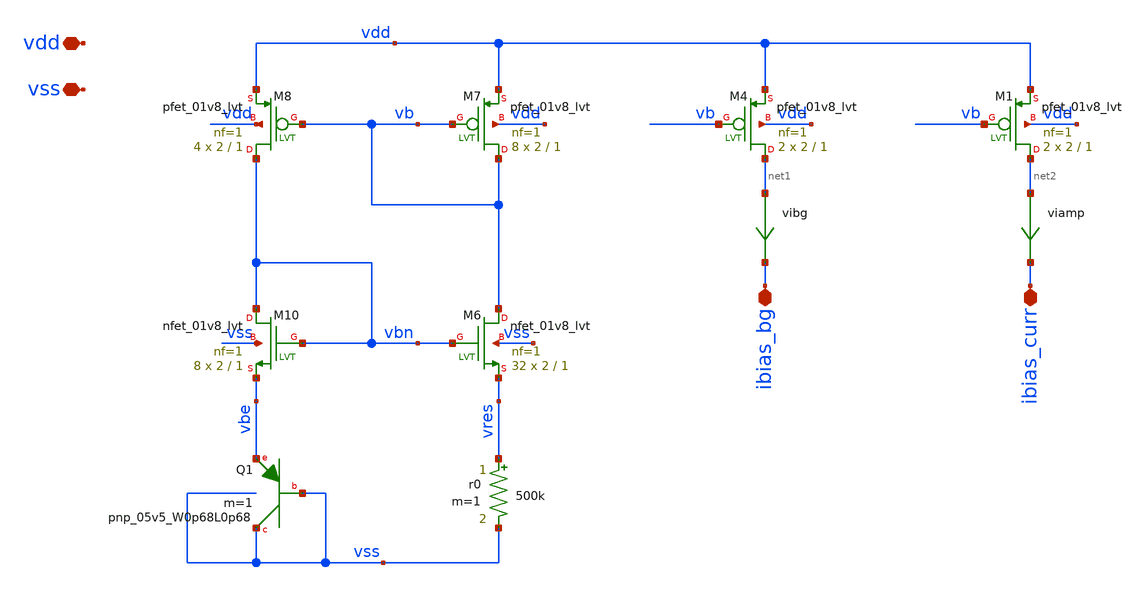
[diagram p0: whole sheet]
** sch_path: xschem/bias/bias_base_p.sch
**.subckt bias_base_p ibias_bg ibias_curr vdd vss
*.iopin ibias_bg
*.iopin ibias_curr
*.iopin vdd
*.iopin vss
r0 vres vss 500k m=1
XQ1 vss vss vbe sky130_fd_pr__pnp_05v5_W0p68L0p68 m=1
XM10 vbn vbn vbe vss sky130_fd_pr__nfet_01v8_lvt L=1 W=2 nf=1 ad='int((nf+1)/2) * W/nf * 0.29' as='int((nf+2)/2) * W/nf * 0.29'
+ pd='2*int((nf+1)/2) * (W/nf + 0.29)' ps='2*int((nf+2)/2) * (W/nf + 0.29)' nrd='0.29 / W' nrs='0.29 / W'
+ sa=0 sb=0 sd=0 mult=8 m=8
XM6 vb vbn vres vss sky130_fd_pr__nfet_01v8_lvt L=1 W=2 nf=1 ad='int((nf+1)/2) * W/nf * 0.29' as='int((nf+2)/2) * W/nf * 0.29'
+ pd='2*int((nf+1)/2) * (W/nf + 0.29)' ps='2*int((nf+2)/2) * (W/nf + 0.29)' nrd='0.29 / W' nrs='0.29 / W'
+ sa=0 sb=0 sd=0 mult=32 m=32
XM7 vb vb vdd vdd sky130_fd_pr__pfet_01v8_lvt L=1 W=2 nf=1 ad='int((nf+1)/2) * W/nf * 0.29' as='int((nf+2)/2) * W/nf * 0.29'
+ pd='2*int((nf+1)/2) * (W/nf + 0.29)' ps='2*int((nf+2)/2) * (W/nf + 0.29)' nrd='0.29 / W' nrs='0.29 / W'
+ sa=0 sb=0 sd=0 mult=8 m=8
XM8 vbn vb vdd vdd sky130_fd_pr__pfet_01v8_lvt L=1 W=2 nf=1 ad='int((nf+1)/2) * W/nf * 0.29' as='int((nf+2)/2) * W/nf * 0.29'
+ pd='2*int((nf+1)/2) * (W/nf + 0.29)' ps='2*int((nf+2)/2) * (W/nf + 0.29)' nrd='0.29 / W' nrs='0.29 / W'
+ sa=0 sb=0 sd=0 mult=4 m=4
XM4 net1 vb vdd vdd sky130_fd_pr__pfet_01v8_lvt L=1 W=2 nf=1 ad='int((nf+1)/2) * W/nf * 0.29' as='int((nf+2)/2) * W/nf * 0.29'
+ pd='2*int((nf+1)/2) * (W/nf + 0.29)' ps='2*int((nf+2)/2) * (W/nf + 0.29)' nrd='0.29 / W' nrs='0.29 / W'
+ sa=0 sb=0 sd=0 mult=2 m=2
XM1 net2 vb vdd vdd sky130_fd_pr__pfet_01v8_lvt L=1 W=2 nf=1 ad='int((nf+1)/2) * W/nf * 0.29' as='int((nf+2)/2) * W/nf * 0.29'
+ pd='2*int((nf+1)/2) * (W/nf + 0.29)' ps='2*int((nf+2)/2) * (W/nf + 0.29)' nrd='0.29 / W' nrs='0.29 / W'
+ sa=0 sb=0 sd=0 mult=2 m=2
vibg net1 ibias_bg 0
.save i(vibg)
viamp net2 ibias_curr 0
.save i(viamp)
**.ends
.end
